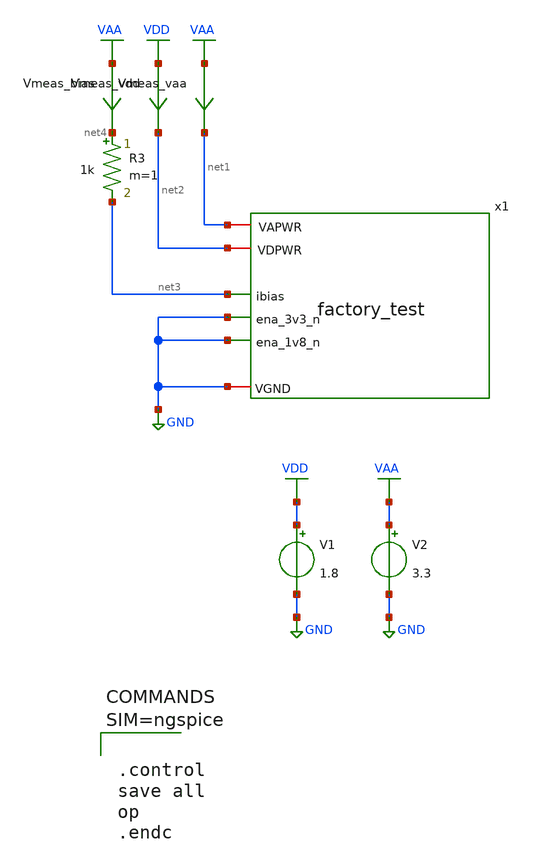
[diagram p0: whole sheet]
** sch_path: tt_um_analog_factory_test/xschem/tb_factory_test.sch
**.subckt tb_factory_test
x1 GND net2 net1 GND GND net3 factory_test
V1 VDD GND 1.8
R3 net4 net3 1k m=1
Vmeas_bias VAA net4 0
V2 VAA GND 3.3
Vmeas_vdd VDD net2 0
Vmeas_vaa VAA net1 0
**** begin user architecture code

** opencircuitdesign pdks install
.lib $::SKYWATER_MODELS/sky130.lib.spice tt





.control
save all
op
.endc



**** end user architecture code
**.ends

* expanding   symbol:  factory_test.sym # of pins=6
** sym_path: tt_um_analog_factory_test/xschem/factory_test.sym
** sch_path: tt_um_analog_factory_test/xschem/factory_test.sch
.subckt factory_test VGND VDPWR VAPWR ena_1v8_n ena_3v3_n ibias
*.ipin ena_3v3_n
*.iopin VDPWR
*.iopin VGND
*.ipin ibias
*.iopin VAPWR
*.ipin ena_1v8_n
XR1 bias ibias VGND sky130_fd_pr__res_high_po_5p73 L=20 mult=1 m=1
XM1 bias bias VGND VGND sky130_fd_pr__nfet_g5v0d10v5 L=0.5 W=16 nf=4 ad='int((nf+1)/2) * W/nf * 0.29'
+ as='int((nf+2)/2) * W/nf * 0.29' pd='2*int((nf+1)/2) * (W/nf + 0.29)' ps='2*int((nf+2)/2) * (W/nf + 0.29)'
+ nrd='0.29 / W' nrs='0.29 / W' sa=0 sb=0 sd=0 mult=1 m=1
XM2 mid_1v8 bias VGND VGND sky130_fd_pr__nfet_g5v0d10v5 L=0.5 W=320 nf=80 ad='int((nf+1)/2) * W/nf * 0.29'
+ as='int((nf+2)/2) * W/nf * 0.29' pd='2*int((nf+1)/2) * (W/nf + 0.29)' ps='2*int((nf+2)/2) * (W/nf + 0.29)'
+ nrd='0.29 / W' nrs='0.29 / W' sa=0 sb=0 sd=0 mult=1 m=1
XM3 mid_3v3 bias VGND VGND sky130_fd_pr__nfet_g5v0d10v5 L=0.5 W=320 nf=80 ad='int((nf+1)/2) * W/nf * 0.29'
+ as='int((nf+2)/2) * W/nf * 0.29' pd='2*int((nf+1)/2) * (W/nf + 0.29)' ps='2*int((nf+2)/2) * (W/nf + 0.29)'
+ nrd='0.29 / W' nrs='0.29 / W' sa=0 sb=0 sd=0 mult=1 m=1
x1 VGND VDPWR VAPWR ena_3v3_n H_ena_3v3_n net1 lv2hv
XM5 mid_3v3 H_ena_3v3_n VAPWR VAPWR sky130_fd_pr__pfet_g5v0d10v5 L=0.5 W=240 nf=80 ad='int((nf+1)/2) * W/nf * 0.29'
+ as='int((nf+2)/2) * W/nf * 0.29' pd='2*int((nf+1)/2) * (W/nf + 0.29)' ps='2*int((nf+2)/2) * (W/nf + 0.29)'
+ nrd='0.29 / W' nrs='0.29 / W' sa=0 sb=0 sd=0 mult=1 m=1
XM4 mid_1v8 ena_1v8_n VDPWR VDPWR sky130_fd_pr__pfet_01v8 L=0.15 W=360 nf=120 ad='int((nf+1)/2) * W/nf * 0.29'
+ as='int((nf+2)/2) * W/nf * 0.29' pd='2*int((nf+1)/2) * (W/nf + 0.29)' ps='2*int((nf+2)/2) * (W/nf + 0.29)'
+ nrd='0.29 / W' nrs='0.29 / W' sa=0 sb=0 sd=0 mult=1 m=1
.ends


* expanding   symbol:  lv2hv.sym # of pins=6
** sym_path: tt_um_analog_factory_test/xschem/lv2hv.sym
** sch_path: tt_um_analog_factory_test/xschem/lv2hv.sch
.subckt lv2hv VGND LVPWR HVPWR in_p H_out_p H_out_n
*.ipin in_p
*.iopin VGND
*.iopin LVPWR
*.iopin HVPWR
*.opin H_out_p
*.opin H_out_n
XM12 H_out_p net2 HVPWR HVPWR sky130_fd_pr__pfet_g5v0d10v5 L=0.5 W=0.84 nf=2 ad='int((nf+1)/2) * W/nf * 0.29'
+ as='int((nf+2)/2) * W/nf * 0.29' pd='2*int((nf+1)/2) * (W/nf + 0.29)' ps='2*int((nf+2)/2) * (W/nf + 0.29)'
+ nrd='0.29 / W' nrs='0.29 / W' sa=0 sb=0 sd=0 mult=1 m=1
XM10 H_out_p net2 VGND VGND sky130_fd_pr__nfet_g5v0d10v5 L=0.5 W=0.42 nf=1 ad='int((nf+1)/2) * W/nf * 0.29'
+ as='int((nf+2)/2) * W/nf * 0.29' pd='2*int((nf+1)/2) * (W/nf + 0.29)' ps='2*int((nf+2)/2) * (W/nf + 0.29)'
+ nrd='0.29 / W' nrs='0.29 / W' sa=0 sb=0 sd=0 mult=1 m=1
XM11 H_out_n net1 HVPWR HVPWR sky130_fd_pr__pfet_g5v0d10v5 L=0.5 W=0.84 nf=2 ad='int((nf+1)/2) * W/nf * 0.29'
+ as='int((nf+2)/2) * W/nf * 0.29' pd='2*int((nf+1)/2) * (W/nf + 0.29)' ps='2*int((nf+2)/2) * (W/nf + 0.29)'
+ nrd='0.29 / W' nrs='0.29 / W' sa=0 sb=0 sd=0 mult=1 m=1
XM9 H_out_n net1 VGND VGND sky130_fd_pr__nfet_g5v0d10v5 L=0.5 W=0.42 nf=1 ad='int((nf+1)/2) * W/nf * 0.29'
+ as='int((nf+2)/2) * W/nf * 0.29' pd='2*int((nf+1)/2) * (W/nf + 0.29)' ps='2*int((nf+2)/2) * (W/nf + 0.29)'
+ nrd='0.29 / W' nrs='0.29 / W' sa=0 sb=0 sd=0 mult=1 m=1
XM1 in_n in_p VGND VGND sky130_fd_pr__nfet_01v8 L=0.15 W=0.42 nf=1 ad='int((nf+1)/2) * W/nf * 0.29' as='int((nf+2)/2) * W/nf * 0.29'
+ pd='2*int((nf+1)/2) * (W/nf + 0.29)' ps='2*int((nf+2)/2) * (W/nf + 0.29)' nrd='0.29 / W' nrs='0.29 / W'
+ sa=0 sb=0 sd=0 mult=1 m=1
XM2 in_n in_p LVPWR LVPWR sky130_fd_pr__pfet_01v8_hvt L=0.15 W=1 nf=1 ad='int((nf+1)/2) * W/nf * 0.29'
+ as='int((nf+2)/2) * W/nf * 0.29' pd='2*int((nf+1)/2) * (W/nf + 0.29)' ps='2*int((nf+2)/2) * (W/nf + 0.29)'
+ nrd='0.29 / W' nrs='0.29 / W' sa=0 sb=0 sd=0 mult=1 m=1
XM3 net1 in_n VGND VGND sky130_fd_pr__nfet_g5v0d10v5 L=0.5 W=0.42 nf=1 ad='int((nf+1)/2) * W/nf * 0.29'
+ as='int((nf+2)/2) * W/nf * 0.29' pd='2*int((nf+1)/2) * (W/nf + 0.29)' ps='2*int((nf+2)/2) * (W/nf + 0.29)'
+ nrd='0.29 / W' nrs='0.29 / W' sa=0 sb=0 sd=0 mult=1 m=1
XM4 net2 in_p VGND VGND sky130_fd_pr__nfet_g5v0d10v5 L=0.5 W=0.42 nf=1 ad='int((nf+1)/2) * W/nf * 0.29'
+ as='int((nf+2)/2) * W/nf * 0.29' pd='2*int((nf+1)/2) * (W/nf + 0.29)' ps='2*int((nf+2)/2) * (W/nf + 0.29)'
+ nrd='0.29 / W' nrs='0.29 / W' sa=0 sb=0 sd=0 mult=1 m=1
XM5 net1 net2 net3 HVPWR sky130_fd_pr__pfet_g5v0d10v5 L=0.5 W=0.42 nf=1 ad='int((nf+1)/2) * W/nf * 0.29'
+ as='int((nf+2)/2) * W/nf * 0.29' pd='2*int((nf+1)/2) * (W/nf + 0.29)' ps='2*int((nf+2)/2) * (W/nf + 0.29)'
+ nrd='0.29 / W' nrs='0.29 / W' sa=0 sb=0 sd=0 mult=1 m=1
XM6 net2 net1 net4 HVPWR sky130_fd_pr__pfet_g5v0d10v5 L=0.5 W=0.42 nf=1 ad='int((nf+1)/2) * W/nf * 0.29'
+ as='int((nf+2)/2) * W/nf * 0.29' pd='2*int((nf+1)/2) * (W/nf + 0.29)' ps='2*int((nf+2)/2) * (W/nf + 0.29)'
+ nrd='0.29 / W' nrs='0.29 / W' sa=0 sb=0 sd=0 mult=1 m=1
XM7 net3 net1 HVPWR HVPWR sky130_fd_pr__pfet_g5v0d10v5 L=0.5 W=0.42 nf=1 ad='int((nf+1)/2) * W/nf * 0.29'
+ as='int((nf+2)/2) * W/nf * 0.29' pd='2*int((nf+1)/2) * (W/nf + 0.29)' ps='2*int((nf+2)/2) * (W/nf + 0.29)'
+ nrd='0.29 / W' nrs='0.29 / W' sa=0 sb=0 sd=0 mult=1 m=1
XM8 net4 net2 HVPWR HVPWR sky130_fd_pr__pfet_g5v0d10v5 L=0.5 W=0.42 nf=1 ad='int((nf+1)/2) * W/nf * 0.29'
+ as='int((nf+2)/2) * W/nf * 0.29' pd='2*int((nf+1)/2) * (W/nf + 0.29)' ps='2*int((nf+2)/2) * (W/nf + 0.29)'
+ nrd='0.29 / W' nrs='0.29 / W' sa=0 sb=0 sd=0 mult=1 m=1
.ends

.GLOBAL GND
.GLOBAL VDD
.GLOBAL VAA
.end
